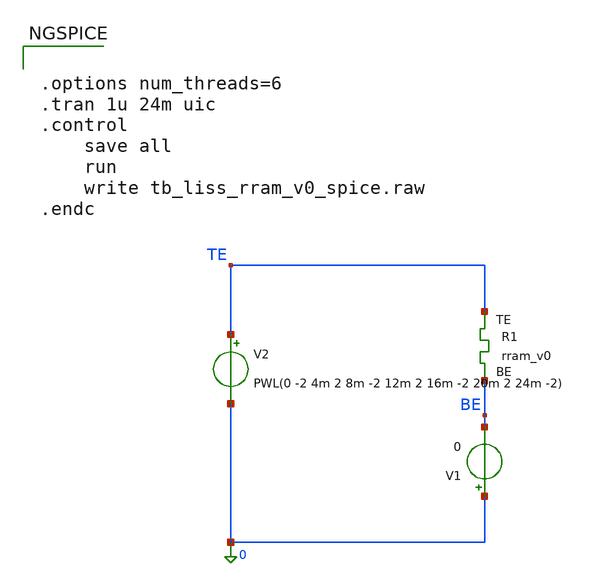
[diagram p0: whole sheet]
** sch_path: memristor_models/wellposed/tb_liss_rram_v0_spice.sch
**.subckt tb_liss_rram_v0_spice
XR1 TE BE rram_v0
V2 TE 0 PWL(0 -2 4m 2 8m -2 12m 2 16m -2 20m 2 24m -2)
V1 0 BE 0
**** begin user architecture code


.options num_threads=6
.tran 1u 24m uic
.control
	save all
	run
	write tb_liss_rram_v0_spice.raw
.endc




** opencircuitdesign pdks install
**.inc $::SKYWATER_MODELS/rram_v0.spice
.inc /home/alex/Desktop/EDA/SNN_IPN/memristor_models/wellposed/wllpsd.spice


**** end user architecture code
**.ends
.end
